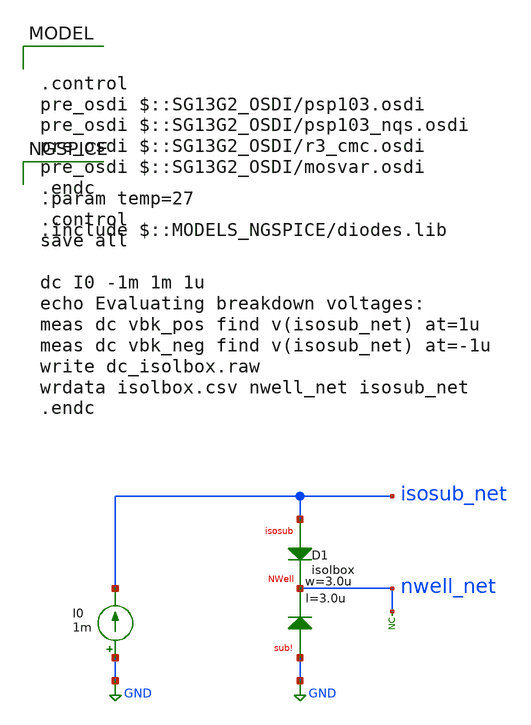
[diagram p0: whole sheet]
** sch_path: ihp-sg13g2/xschem_libs/sg13g2_tests/dc_isolbox/schematic/dc_isolbox.sch
* Copyright 2023 IHP PDK Authors
**.subckt dc_isolbox
I0 GND isosub_net 1m
XD1 isosub_net nwell_net GND isolbox l=3.0u w=3.0u
* noconn nwell_net
**** begin user architecture code

.control
pre_osdi $::SG13G2_OSDI/psp103.osdi
pre_osdi $::SG13G2_OSDI/psp103_nqs.osdi
pre_osdi $::SG13G2_OSDI/r3_cmc.osdi
pre_osdi $::SG13G2_OSDI/mosvar.osdi
.endc

.include $::MODELS_NGSPICE/diodes.lib



.param temp=27
.control
save all

dc I0 -1m 1m 1u
echo Evaluating breakdown voltages:
meas dc vbk_pos find v(isosub_net) at=1u
meas dc vbk_neg find v(isosub_net) at=-1u
write dc_isolbox.raw
wrdata isolbox.csv nwell_net isosub_net
.endc


**** end user architecture code
**.ends
.GLOBAL GND
.end
